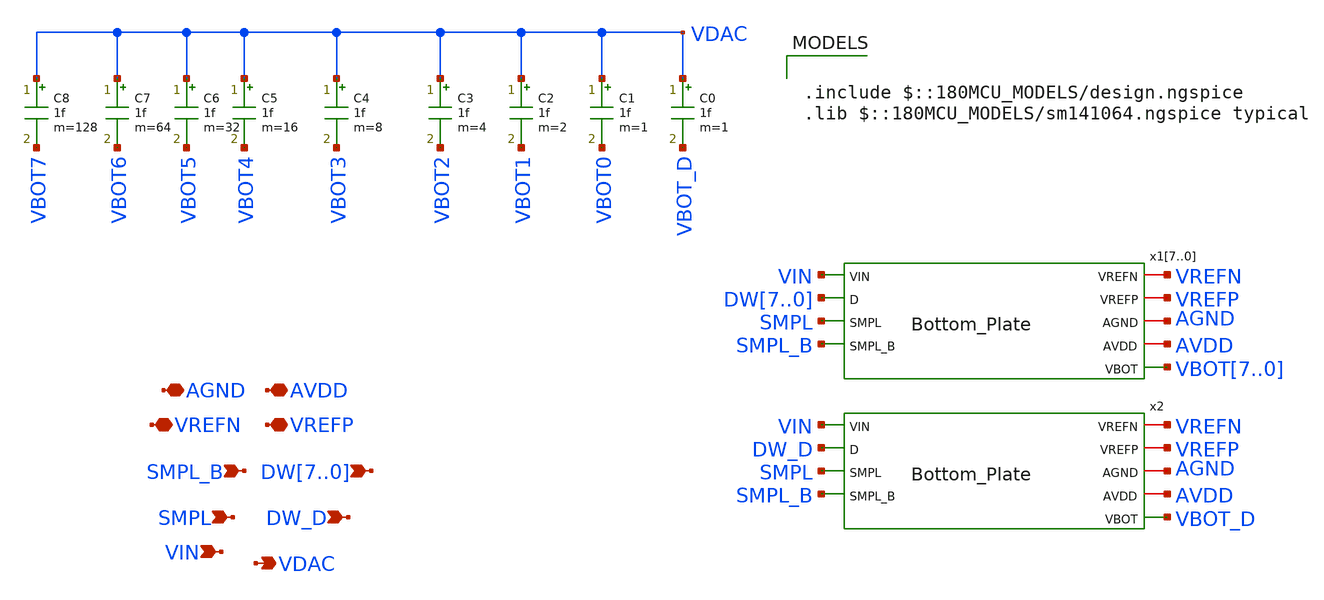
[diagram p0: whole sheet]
** sch_path: XSCHEM Files/Cap_DAC.sch
**.subckt Cap_DAC AVDD VREFP VREFN VIN SMPL_B SMPL VDAC DW7,DW6,DW5,DW4,DW3,DW2,DW1,DW0 DW_D AGND
*.iopin AVDD
*.iopin VREFP
*.iopin VREFN
*.ipin VIN
*.ipin SMPL_B
*.ipin SMPL
*.opin VDAC
*.ipin DW7,DW6,DW5,DW4,DW3,DW2,DW1,DW0
*.ipin DW_D
*.iopin AGND
C0 VDAC VBOT_D 1f m=1
C1 VDAC VBOT0 1f m=1
C2 VDAC VBOT1 1f m=2
C3 VDAC VBOT2 1f m=4
C4 VDAC VBOT3 1f m=8
C5 VDAC VBOT4 1f m=16
C6 VDAC VBOT5 1f m=32
C7 VDAC VBOT6 1f m=64
C8 VDAC VBOT7 1f m=128
x17 VREFN VREFP AGND AVDD VIN DW7 SMPL SMPL_B VBOT7 Bottom_Plate
x16 VREFN VREFP AGND AVDD VIN DW6 SMPL SMPL_B VBOT6 Bottom_Plate
x15 VREFN VREFP AGND AVDD VIN DW5 SMPL SMPL_B VBOT5 Bottom_Plate
x14 VREFN VREFP AGND AVDD VIN DW4 SMPL SMPL_B VBOT4 Bottom_Plate
x13 VREFN VREFP AGND AVDD VIN DW3 SMPL SMPL_B VBOT3 Bottom_Plate
x12 VREFN VREFP AGND AVDD VIN DW2 SMPL SMPL_B VBOT2 Bottom_Plate
x11 VREFN VREFP AGND AVDD VIN DW1 SMPL SMPL_B VBOT1 Bottom_Plate
x10 VREFN VREFP AGND AVDD VIN DW0 SMPL SMPL_B VBOT0 Bottom_Plate
x2 VREFN VREFP AGND AVDD VIN DW_D SMPL SMPL_B VBOT_D Bottom_Plate
**** begin user architecture code

.include $::180MCU_MODELS/design.ngspice
.lib $::180MCU_MODELS/sm141064.ngspice typical

**** end user architecture code
**.ends

* expanding   symbol:  /home/tare/Desktop/last/Bottom_Plate.sym # of pins=9
** sym_path: XSCHEM Files/Bottom_Plate.sym
** sch_path: XSCHEM Files/Bottom_Plate.sch
.subckt Bottom_Plate VREFN VREFP AGND AVDD VIN D SMPL SMPL_B VBOT
*.iopin AGND
*.iopin AVDD
*.iopin VREFP
*.iopin VREFN
*.opin VBOT
*.ipin VIN
*.ipin D
*.ipin SMPL_B
*.ipin SMPL
XM1 VBOT net1 VREFN AGND nmos_3p3 L=0.28u W=5u nf=1 ad='int((nf+1)/2) * W/nf * 0.18u' as='int((nf+2)/2) * W/nf * 0.18u'
+ pd='2*int((nf+1)/2) * (W/nf + 0.18u)' ps='2*int((nf+2)/2) * (W/nf + 0.18u)' nrd='0.18u / W' nrs='0.18u / W'
+ sa=0 sb=0 sd=0 m=1
XM2 VREFP net2 VBOT AVDD pmos_3p3 L=0.28u W=10u nf=1 ad='int((nf+1)/2) * W/nf * 0.18u' as='int((nf+2)/2) * W/nf * 0.18u'
+ pd='2*int((nf+1)/2) * (W/nf + 0.18u)' ps='2*int((nf+2)/2) * (W/nf + 0.18u)' nrd='0.18u / W' nrs='0.18u / W'
+ sa=0 sb=0 sd=0 m=1
x2 net1 D SMPL nor
x3 net2 D SMPL_B nand
x1 SMPL AGND VBOT VIN AVDD tg
.ends


* expanding   symbol:  /home/tare/Desktop/Final_1/nor.sym # of pins=3
** sym_path: XSCHEM Files/nor.sym
** sch_path: XSCHEM Files/nor.sch
.subckt nor Y A B
*.ipin A
*.opin Y
*.ipin B
**** begin user architecture code


*nor model
a1 [A b] Yi my_nor
.model my_nor d_nor(rise_delay = 1e-9 fall_delay = 1e-9                         input_load = 1e-12)

*force netlisting of digital outputs
v1 Yi Y 0


**** end user architecture code
.ends


* expanding   symbol:  /home/tare/Desktop/Final_1/nand.sym # of pins=3
** sym_path: XSCHEM Files/nand.sym
** sch_path: XSCHEM Files/nand.sch
.subckt nand Y A B
*.ipin A
*.opin Y
*.ipin B
**** begin user architecture code


*nand model
a1 [A b] Yi my_nand
.model my_nand d_nand(rise_delay = 1e-9 fall_delay = 1e-9                         input_load =
+ 1e-12)

*force netlisting of digital outputs
v1 Yi Y 0


**** end user architecture code
.ends


* expanding   symbol:  /home/tare/Desktop/last/tg.sym # of pins=5
** sym_path: XSCHEM Files/tg.sym
** sch_path: XSCHEM Files/tg.sch
.subckt tg EN AGND VOUT VIN AVDD
*.iopin AGND
*.iopin AVDD
*.iopin VOUT
*.iopin VIN
*.iopin EN
XM1 VOUT EN VIN AGND nmos_3p3 L=0.28u W=5u nf=1 ad='int((nf+1)/2) * W/nf * 0.18u' as='int((nf+2)/2) * W/nf * 0.18u'
+ pd='2*int((nf+1)/2) * (W/nf + 0.18u)' ps='2*int((nf+2)/2) * (W/nf + 0.18u)' nrd='0.18u / W' nrs='0.18u / W'
+ sa=0 sb=0 sd=0 m=1
XM2 VOUT ENB VIN AVDD pmos_3p3 L=0.28u W=10u nf=1 ad='int((nf+1)/2) * W/nf * 0.18u' as='int((nf+2)/2) * W/nf * 0.18u'
+ pd='2*int((nf+1)/2) * (W/nf + 0.18u)' ps='2*int((nf+2)/2) * (W/nf + 0.18u)' nrd='0.18u / W' nrs='0.18u / W'
+ sa=0 sb=0 sd=0 m=1
E1 ENB AVDD EN AGND -1
.ends

.end
